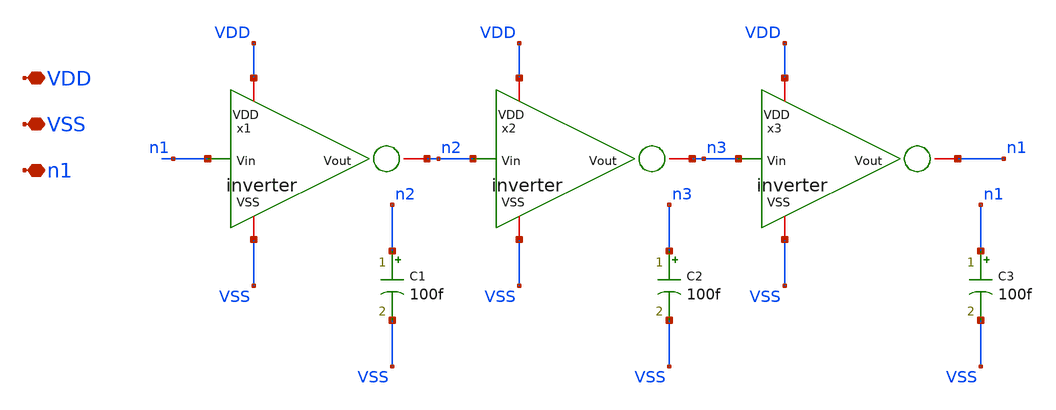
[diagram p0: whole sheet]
** sch_path: gf180_examples/RO/xschem/3_stage_RO.sch
**.subckt 3_stage_RO VDD VSS n1
*.iopin VDD
*.iopin VSS
*.iopin n1
x1 n1 VDD VSS n2 inverter
x2 n2 VDD VSS n3 inverter
x3 n3 VDD VSS n1 inverter
C1 n2 VSS 100f m=1
C2 n3 VSS 100f m=1
C3 n1 VSS 100f m=1
**.ends

* expanding   symbol:  /foss/designs/Chipathon2025_gf180/gf180_examples/inverter/xschem/inverter.sym
*+ # of pins=4
** sym_path: gf180_examples/inverter/xschem/inverter.sym
** sch_path: gf180_examples/inverter/xschem/inverter.sch
.subckt inverter Vin VDD VSS Vout
*.ipin Vin
*.iopin VDD
*.iopin VSS
*.iopin Vout
XM1 Vout Vin VSS VSS nfet_03v3 L=1u W=3u nf=1 ad='int((nf+1)/2) * W/nf * 0.18u' as='int((nf+2)/2) * W/nf * 0.18u'
+ pd='2*int((nf+1)/2) * (W/nf + 0.18u)' ps='2*int((nf+2)/2) * (W/nf + 0.18u)' nrd='0.18u / W' nrs='0.18u / W'
+ sa=0 sb=0 sd=0 m=1
XM2 Vout Vin VDD VDD pfet_03v3 L=1u W=3u nf=1 ad='int((nf+1)/2) * W/nf * 0.18u' as='int((nf+2)/2) * W/nf * 0.18u'
+ pd='2*int((nf+1)/2) * (W/nf + 0.18u)' ps='2*int((nf+2)/2) * (W/nf + 0.18u)' nrd='0.18u / W' nrs='0.18u / W'
+ sa=0 sb=0 sd=0 m=1
.ends

.end
